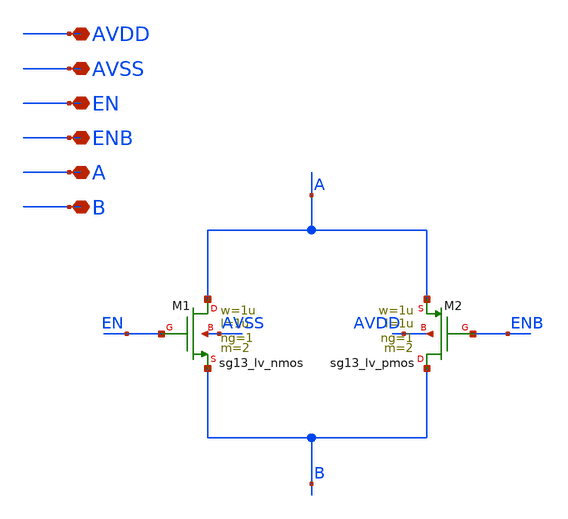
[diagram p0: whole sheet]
** sch_path: current_generator/analog/DAC/schematics/tgate_gold.sch
**.subckt tgate_gold AVDD AVSS EN ENB A B
*.iopin AVDD
*.iopin AVSS
*.iopin EN
*.iopin ENB
*.iopin A
*.iopin B
XM1 A EN B AVSS sg13_lv_nmos w=1u l=1u ng=1 m=2 mm_ok=1
XM2 B ENB A AVDD sg13_lv_pmos w=1u l=1u ng=1 m=2 mm_ok=1
**.ends
.end
